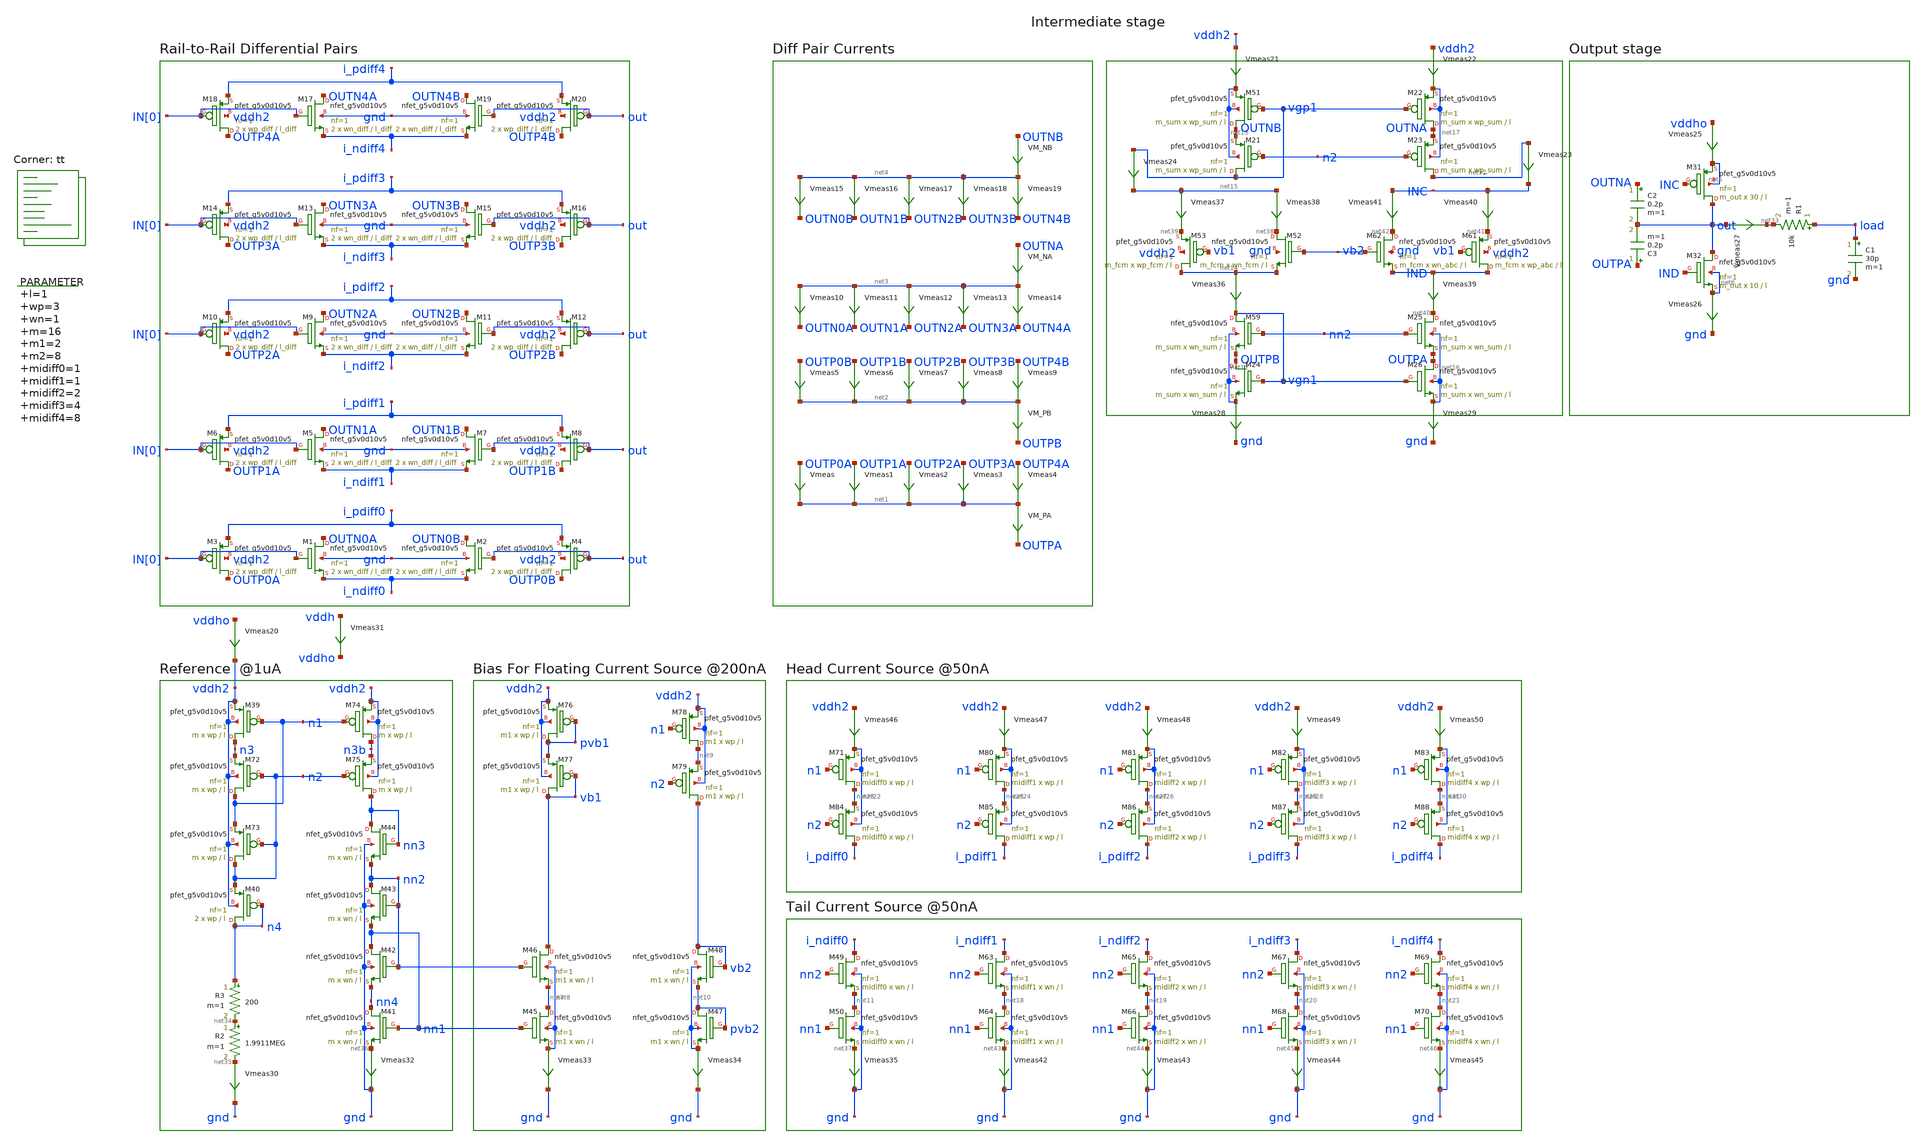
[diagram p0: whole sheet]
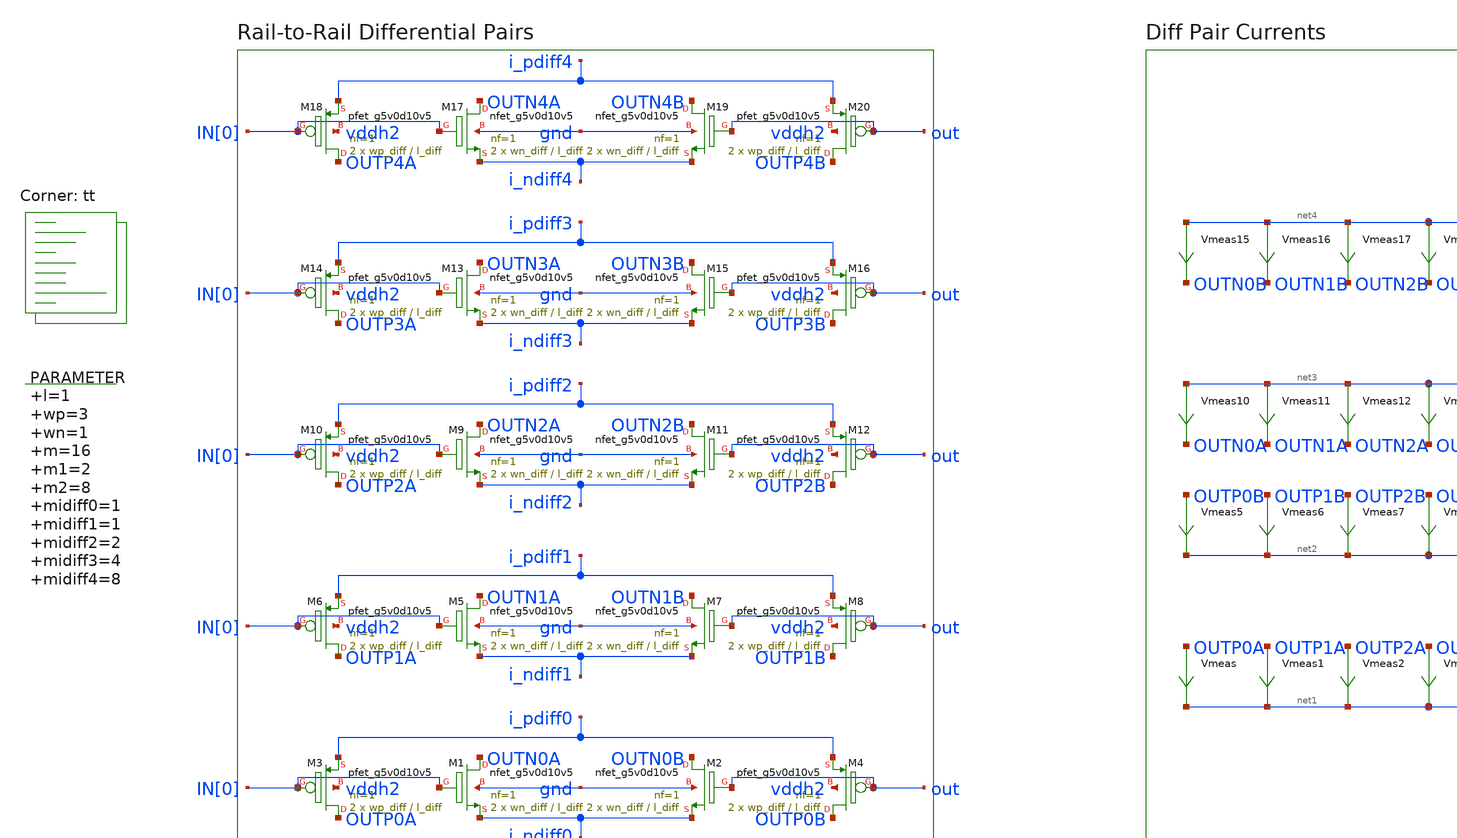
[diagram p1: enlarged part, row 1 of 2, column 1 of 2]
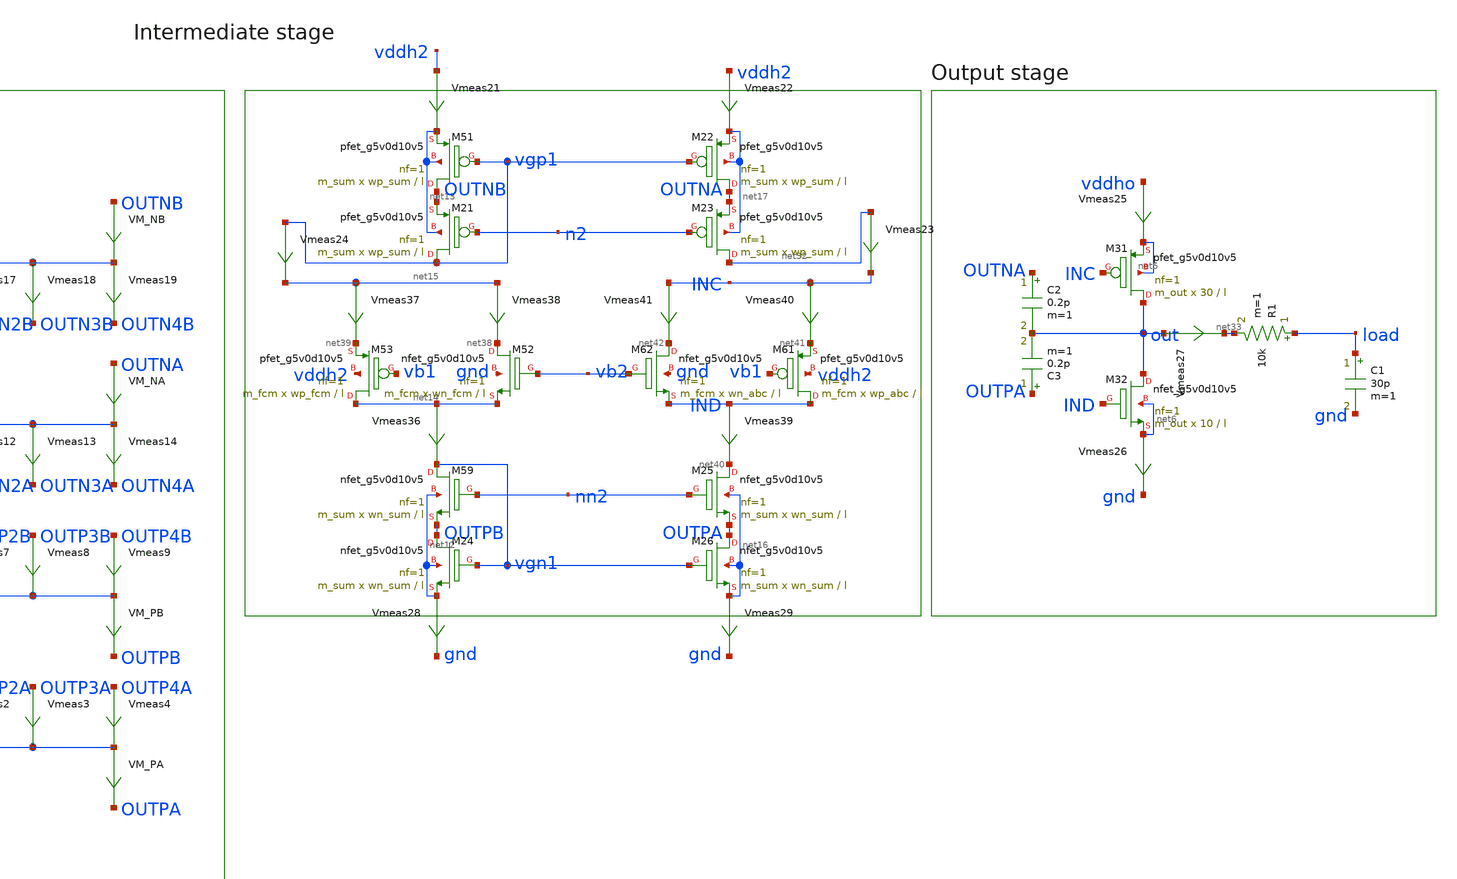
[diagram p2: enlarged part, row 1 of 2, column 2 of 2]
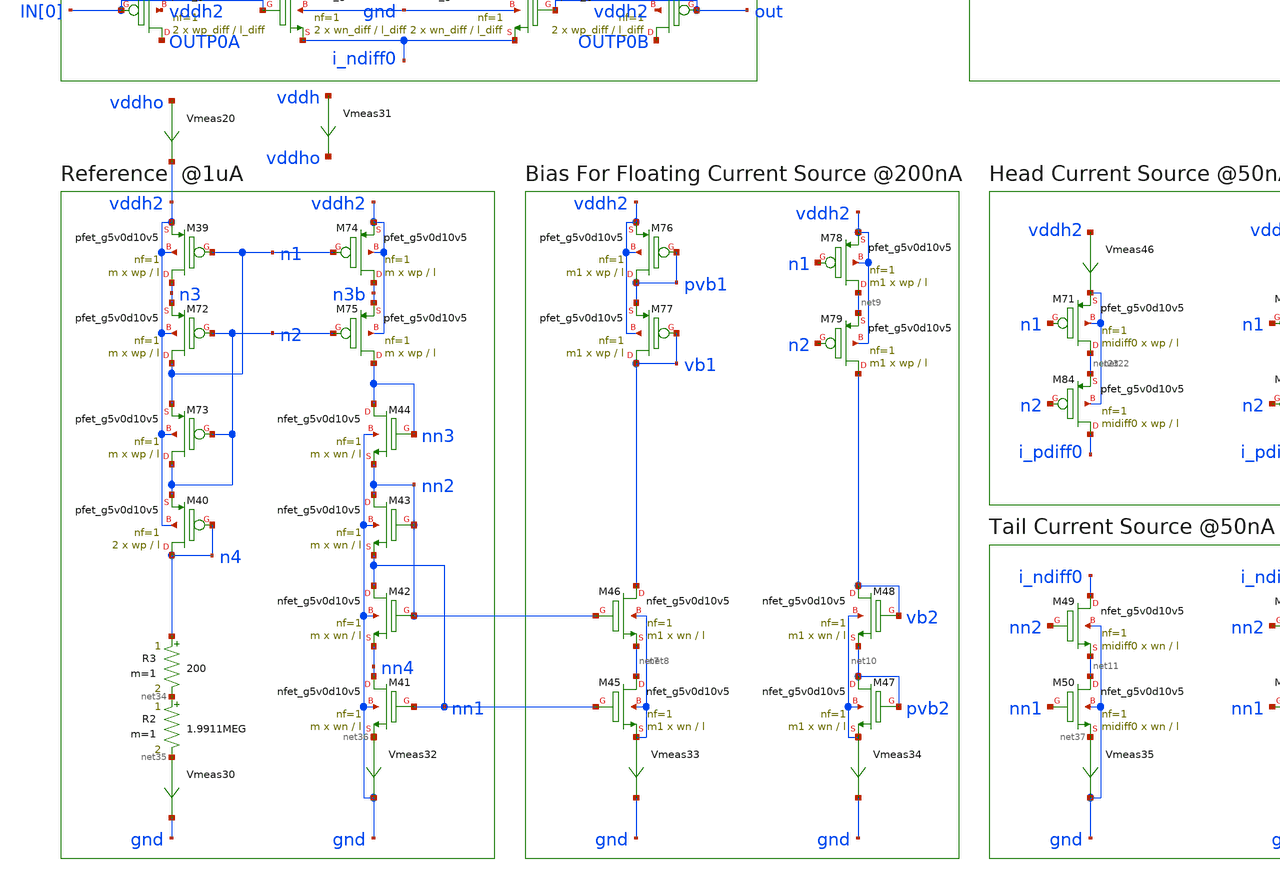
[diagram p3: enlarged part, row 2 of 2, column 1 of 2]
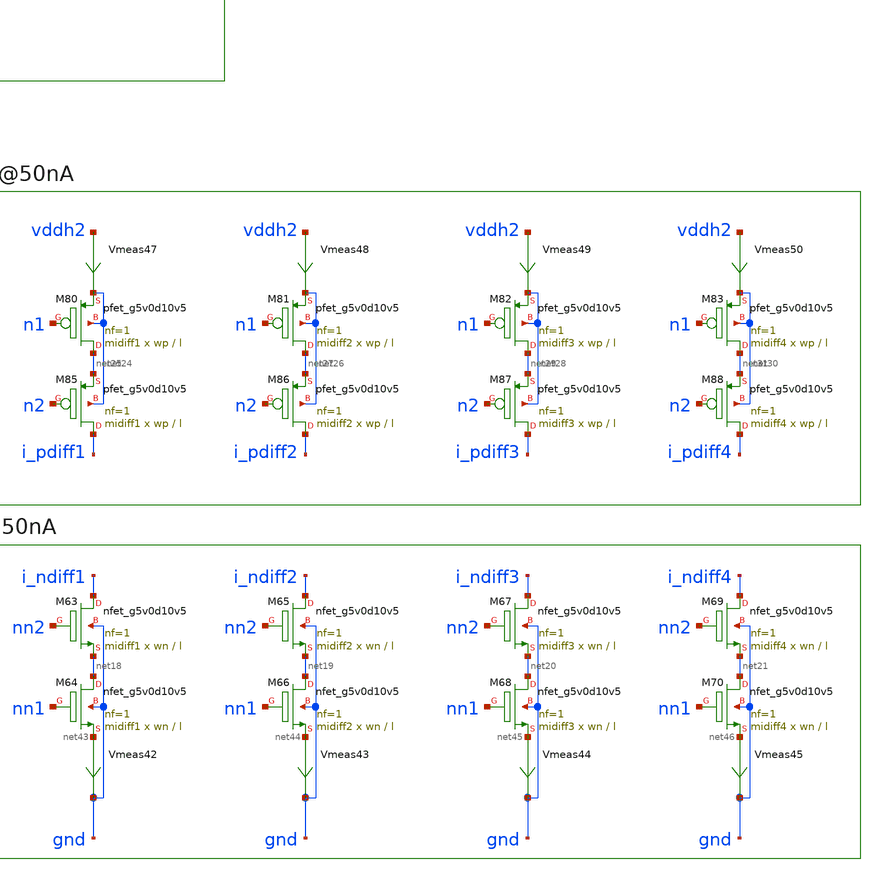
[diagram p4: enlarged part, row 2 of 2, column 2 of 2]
** sch_path: xschem/op_amp_v2-tb.sch
**.subckt op_amp_v2-tb
XM1 OUTN0A IN[0] i_ndiff0 gnd sky130_fd_pr__nfet_g5v0d10v5 L=l_diff W=wn_diff nf=1 ad='int((nf+1)/2) * W/nf * 0.29'
+ as='int((nf+2)/2) * W/nf * 0.29' pd='2*int((nf+1)/2) * (W/nf + 0.29)' ps='2*int((nf+2)/2) * (W/nf + 0.29)'
+ nrd='0.29 / W' nrs='0.29 / W' sa=0 sb=0 sd=0 mult=2 m=2
XM3 OUTP0A IN[0] i_pdiff0 vddh2 sky130_fd_pr__pfet_g5v0d10v5 L=l_diff W=wp_diff nf=1 ad='int((nf+1)/2) * W/nf * 0.29'
+ as='int((nf+2)/2) * W/nf * 0.29' pd='2*int((nf+1)/2) * (W/nf + 0.29)' ps='2*int((nf+2)/2) * (W/nf + 0.29)'
+ nrd='0.29 / W' nrs='0.29 / W' sa=0 sb=0 sd=0 mult=2 m=2
Vmeas OUTP0A net1 0
.save i(vmeas)
Vmeas1 OUTP1A net1 0
.save i(vmeas1)
Vmeas2 OUTP2A net1 0
.save i(vmeas2)
Vmeas3 OUTP3A net1 0
.save i(vmeas3)
Vmeas4 OUTP4A net1 0
.save i(vmeas4)
Vmeas5 OUTP0B net2 0
.save i(vmeas5)
Vmeas6 OUTP1B net2 0
.save i(vmeas6)
Vmeas7 OUTP2B net2 0
.save i(vmeas7)
Vmeas8 OUTP3B net2 0
.save i(vmeas8)
Vmeas9 OUTP4B net2 0
.save i(vmeas9)
Vmeas10 net3 OUTN0A 0
.save i(vmeas10)
Vmeas11 net3 OUTN1A 0
.save i(vmeas11)
Vmeas12 net3 OUTN2A 0
.save i(vmeas12)
Vmeas13 net3 OUTN3A 0
.save i(vmeas13)
Vmeas14 net3 OUTN4A 0
.save i(vmeas14)
Vmeas15 net4 OUTN0B 0
.save i(vmeas15)
Vmeas16 net4 OUTN1B 0
.save i(vmeas16)
Vmeas17 net4 OUTN2B 0
.save i(vmeas17)
Vmeas18 net4 OUTN3B 0
.save i(vmeas18)
Vmeas19 net4 OUTN4B 0
.save i(vmeas19)
XM31 out INC net5 net5 sky130_fd_pr__pfet_g5v0d10v5 L=l W=30 nf=1 ad='int((nf+1)/2) * W/nf * 0.29' as='int((nf+2)/2) * W/nf * 0.29'
+ pd='2*int((nf+1)/2) * (W/nf + 0.29)' ps='2*int((nf+2)/2) * (W/nf + 0.29)' nrd='0.29 / W' nrs='0.29 / W'
+ sa=0 sb=0 sd=0 mult=m_out m=m_out
XM32 out IND net6 net6 sky130_fd_pr__nfet_g5v0d10v5 L=l W=10 nf=1 ad='int((nf+1)/2) * W/nf * 0.29' as='int((nf+2)/2) * W/nf * 0.29'
+ pd='2*int((nf+1)/2) * (W/nf + 0.29)' ps='2*int((nf+2)/2) * (W/nf + 0.29)' nrd='0.29 / W' nrs='0.29 / W'
+ sa=0 sb=0 sd=0 mult=m_out m=m_out
R1 load net33 10k m=1
Vmeas25 vddho net5 0
.save i(vmeas25)
Vmeas26 net6 gnd 0
.save i(vmeas26)
C1 load gnd 30p m=1
VM_NB OUTNB net4 0
.save i(vm_nb)
VM_NA OUTNA net3 0
.save i(vm_na)
VM_PB net2 OUTPB 0
.save i(vm_pb)
VM_PA net1 OUTPA 0
.save i(vm_pa)
C2 OUTNA out 0.2p m=1
C3 OUTPA out 0.2p m=1
XM2 OUTN0B out i_ndiff0 gnd sky130_fd_pr__nfet_g5v0d10v5 L=l_diff W=wn_diff nf=1 ad='int((nf+1)/2) * W/nf * 0.29'
+ as='int((nf+2)/2) * W/nf * 0.29' pd='2*int((nf+1)/2) * (W/nf + 0.29)' ps='2*int((nf+2)/2) * (W/nf + 0.29)'
+ nrd='0.29 / W' nrs='0.29 / W' sa=0 sb=0 sd=0 mult=2 m=2
XM4 OUTP0B out i_pdiff0 vddh2 sky130_fd_pr__pfet_g5v0d10v5 L=l_diff W=wp_diff nf=1 ad='int((nf+1)/2) * W/nf * 0.29'
+ as='int((nf+2)/2) * W/nf * 0.29' pd='2*int((nf+1)/2) * (W/nf + 0.29)' ps='2*int((nf+2)/2) * (W/nf + 0.29)'
+ nrd='0.29 / W' nrs='0.29 / W' sa=0 sb=0 sd=0 mult=2 m=2
XM5 OUTN1A IN[0] i_ndiff1 gnd sky130_fd_pr__nfet_g5v0d10v5 L=l_diff W=wn_diff nf=1 ad='int((nf+1)/2) * W/nf * 0.29'
+ as='int((nf+2)/2) * W/nf * 0.29' pd='2*int((nf+1)/2) * (W/nf + 0.29)' ps='2*int((nf+2)/2) * (W/nf + 0.29)'
+ nrd='0.29 / W' nrs='0.29 / W' sa=0 sb=0 sd=0 mult=2 m=2
XM6 OUTP1A IN[0] i_pdiff1 vddh2 sky130_fd_pr__pfet_g5v0d10v5 L=l_diff W=wp_diff nf=1 ad='int((nf+1)/2) * W/nf * 0.29'
+ as='int((nf+2)/2) * W/nf * 0.29' pd='2*int((nf+1)/2) * (W/nf + 0.29)' ps='2*int((nf+2)/2) * (W/nf + 0.29)'
+ nrd='0.29 / W' nrs='0.29 / W' sa=0 sb=0 sd=0 mult=2 m=2
XM7 OUTN1B out i_ndiff1 gnd sky130_fd_pr__nfet_g5v0d10v5 L=l_diff W=wn_diff nf=1 ad='int((nf+1)/2) * W/nf * 0.29'
+ as='int((nf+2)/2) * W/nf * 0.29' pd='2*int((nf+1)/2) * (W/nf + 0.29)' ps='2*int((nf+2)/2) * (W/nf + 0.29)'
+ nrd='0.29 / W' nrs='0.29 / W' sa=0 sb=0 sd=0 mult=2 m=2
XM8 OUTP1B out i_pdiff1 vddh2 sky130_fd_pr__pfet_g5v0d10v5 L=l_diff W=wp_diff nf=1 ad='int((nf+1)/2) * W/nf * 0.29'
+ as='int((nf+2)/2) * W/nf * 0.29' pd='2*int((nf+1)/2) * (W/nf + 0.29)' ps='2*int((nf+2)/2) * (W/nf + 0.29)'
+ nrd='0.29 / W' nrs='0.29 / W' sa=0 sb=0 sd=0 mult=2 m=2
XM9 OUTN2A IN[0] i_ndiff2 gnd sky130_fd_pr__nfet_g5v0d10v5 L=l_diff W=wn_diff nf=1 ad='int((nf+1)/2) * W/nf * 0.29'
+ as='int((nf+2)/2) * W/nf * 0.29' pd='2*int((nf+1)/2) * (W/nf + 0.29)' ps='2*int((nf+2)/2) * (W/nf + 0.29)'
+ nrd='0.29 / W' nrs='0.29 / W' sa=0 sb=0 sd=0 mult=2 m=2
XM10 OUTP2A IN[0] i_pdiff2 vddh2 sky130_fd_pr__pfet_g5v0d10v5 L=l_diff W=wp_diff nf=1 ad='int((nf+1)/2) * W/nf * 0.29'
+ as='int((nf+2)/2) * W/nf * 0.29' pd='2*int((nf+1)/2) * (W/nf + 0.29)' ps='2*int((nf+2)/2) * (W/nf + 0.29)'
+ nrd='0.29 / W' nrs='0.29 / W' sa=0 sb=0 sd=0 mult=2 m=2
XM11 OUTN2B out i_ndiff2 gnd sky130_fd_pr__nfet_g5v0d10v5 L=l_diff W=wn_diff nf=1 ad='int((nf+1)/2) * W/nf * 0.29'
+ as='int((nf+2)/2) * W/nf * 0.29' pd='2*int((nf+1)/2) * (W/nf + 0.29)' ps='2*int((nf+2)/2) * (W/nf + 0.29)'
+ nrd='0.29 / W' nrs='0.29 / W' sa=0 sb=0 sd=0 mult=2 m=2
XM12 OUTP2B out i_pdiff2 vddh2 sky130_fd_pr__pfet_g5v0d10v5 L=l_diff W=wp_diff nf=1 ad='int((nf+1)/2) * W/nf * 0.29'
+ as='int((nf+2)/2) * W/nf * 0.29' pd='2*int((nf+1)/2) * (W/nf + 0.29)' ps='2*int((nf+2)/2) * (W/nf + 0.29)'
+ nrd='0.29 / W' nrs='0.29 / W' sa=0 sb=0 sd=0 mult=2 m=2
XM13 OUTN3A IN[0] i_ndiff3 gnd sky130_fd_pr__nfet_g5v0d10v5 L=l_diff W=wn_diff nf=1 ad='int((nf+1)/2) * W/nf * 0.29'
+ as='int((nf+2)/2) * W/nf * 0.29' pd='2*int((nf+1)/2) * (W/nf + 0.29)' ps='2*int((nf+2)/2) * (W/nf + 0.29)'
+ nrd='0.29 / W' nrs='0.29 / W' sa=0 sb=0 sd=0 mult=2 m=2
XM14 OUTP3A IN[0] i_pdiff3 vddh2 sky130_fd_pr__pfet_g5v0d10v5 L=l_diff W=wp_diff nf=1 ad='int((nf+1)/2) * W/nf * 0.29'
+ as='int((nf+2)/2) * W/nf * 0.29' pd='2*int((nf+1)/2) * (W/nf + 0.29)' ps='2*int((nf+2)/2) * (W/nf + 0.29)'
+ nrd='0.29 / W' nrs='0.29 / W' sa=0 sb=0 sd=0 mult=2 m=2
XM15 OUTN3B out i_ndiff3 gnd sky130_fd_pr__nfet_g5v0d10v5 L=l_diff W=wn_diff nf=1 ad='int((nf+1)/2) * W/nf * 0.29'
+ as='int((nf+2)/2) * W/nf * 0.29' pd='2*int((nf+1)/2) * (W/nf + 0.29)' ps='2*int((nf+2)/2) * (W/nf + 0.29)'
+ nrd='0.29 / W' nrs='0.29 / W' sa=0 sb=0 sd=0 mult=2 m=2
XM16 OUTP3B out i_pdiff3 vddh2 sky130_fd_pr__pfet_g5v0d10v5 L=l_diff W=wp_diff nf=1 ad='int((nf+1)/2) * W/nf * 0.29'
+ as='int((nf+2)/2) * W/nf * 0.29' pd='2*int((nf+1)/2) * (W/nf + 0.29)' ps='2*int((nf+2)/2) * (W/nf + 0.29)'
+ nrd='0.29 / W' nrs='0.29 / W' sa=0 sb=0 sd=0 mult=2 m=2
XM17 OUTN4A IN[0] i_ndiff4 gnd sky130_fd_pr__nfet_g5v0d10v5 L=l_diff W=wn_diff nf=1 ad='int((nf+1)/2) * W/nf * 0.29'
+ as='int((nf+2)/2) * W/nf * 0.29' pd='2*int((nf+1)/2) * (W/nf + 0.29)' ps='2*int((nf+2)/2) * (W/nf + 0.29)'
+ nrd='0.29 / W' nrs='0.29 / W' sa=0 sb=0 sd=0 mult=2 m=2
XM18 OUTP4A IN[0] i_pdiff4 vddh2 sky130_fd_pr__pfet_g5v0d10v5 L=l_diff W=wp_diff nf=1 ad='int((nf+1)/2) * W/nf * 0.29'
+ as='int((nf+2)/2) * W/nf * 0.29' pd='2*int((nf+1)/2) * (W/nf + 0.29)' ps='2*int((nf+2)/2) * (W/nf + 0.29)'
+ nrd='0.29 / W' nrs='0.29 / W' sa=0 sb=0 sd=0 mult=2 m=2
XM19 OUTN4B out i_ndiff4 gnd sky130_fd_pr__nfet_g5v0d10v5 L=l_diff W=wn_diff nf=1 ad='int((nf+1)/2) * W/nf * 0.29'
+ as='int((nf+2)/2) * W/nf * 0.29' pd='2*int((nf+1)/2) * (W/nf + 0.29)' ps='2*int((nf+2)/2) * (W/nf + 0.29)'
+ nrd='0.29 / W' nrs='0.29 / W' sa=0 sb=0 sd=0 mult=2 m=2
XM20 OUTP4B out i_pdiff4 vddh2 sky130_fd_pr__pfet_g5v0d10v5 L=l_diff W=wp_diff nf=1 ad='int((nf+1)/2) * W/nf * 0.29'
+ as='int((nf+2)/2) * W/nf * 0.29' pd='2*int((nf+1)/2) * (W/nf + 0.29)' ps='2*int((nf+2)/2) * (W/nf + 0.29)'
+ nrd='0.29 / W' nrs='0.29 / W' sa=0 sb=0 sd=0 mult=2 m=2
XM39 n3 n1 vddh2 vddh2 sky130_fd_pr__pfet_g5v0d10v5 L=l W=wp nf=1 ad='int((nf+1)/2) * W/nf * 0.29' as='int((nf+2)/2) * W/nf * 0.29'
+ pd='2*int((nf+1)/2) * (W/nf + 0.29)' ps='2*int((nf+2)/2) * (W/nf + 0.29)' nrd='0.29 / W' nrs='0.29 / W'
+ sa=0 sb=0 sd=0 mult=m m=m
R2 net34 net35 1.9911MEG m=1
Vmeas30 net35 gnd 0
.save i(vmeas30)
R3 n4 net34 200 m=1
XM40 n4 n4 n2 vddh2 sky130_fd_pr__pfet_g5v0d10v5 L=l W=wp nf=1 ad='int((nf+1)/2) * W/nf * 0.29' as='int((nf+2)/2) * W/nf * 0.29'
+ pd='2*int((nf+1)/2) * (W/nf + 0.29)' ps='2*int((nf+2)/2) * (W/nf + 0.29)' nrd='0.29 / W' nrs='0.29 / W'
+ sa=0 sb=0 sd=0 mult=2 m=2
Vmeas31 vddh vddho 0
.save i(vmeas31)
XM41 nn4 nn1 net36 gnd sky130_fd_pr__nfet_g5v0d10v5 L=l W=wn nf=1 ad='int((nf+1)/2) * W/nf * 0.29' as='int((nf+2)/2) * W/nf * 0.29'
+ pd='2*int((nf+1)/2) * (W/nf + 0.29)' ps='2*int((nf+2)/2) * (W/nf + 0.29)' nrd='0.29 / W' nrs='0.29 / W'
+ sa=0 sb=0 sd=0 mult=m m=m
XM42 nn1 nn2 nn4 gnd sky130_fd_pr__nfet_g5v0d10v5 L=l W=wn nf=1 ad='int((nf+1)/2) * W/nf * 0.29' as='int((nf+2)/2) * W/nf * 0.29'
+ pd='2*int((nf+1)/2) * (W/nf + 0.29)' ps='2*int((nf+2)/2) * (W/nf + 0.29)' nrd='0.29 / W' nrs='0.29 / W'
+ sa=0 sb=0 sd=0 mult=m m=m
XM43 nn2 nn2 nn1 gnd sky130_fd_pr__nfet_g5v0d10v5 L=l W=wn nf=1 ad='int((nf+1)/2) * W/nf * 0.29' as='int((nf+2)/2) * W/nf * 0.29'
+ pd='2*int((nf+1)/2) * (W/nf + 0.29)' ps='2*int((nf+2)/2) * (W/nf + 0.29)' nrd='0.29 / W' nrs='0.29 / W'
+ sa=0 sb=0 sd=0 mult=m m=m
XM44 nn3 nn3 nn2 gnd sky130_fd_pr__nfet_g5v0d10v5 L=l W=wn nf=1 ad='int((nf+1)/2) * W/nf * 0.29' as='int((nf+2)/2) * W/nf * 0.29'
+ pd='2*int((nf+1)/2) * (W/nf + 0.29)' ps='2*int((nf+2)/2) * (W/nf + 0.29)' nrd='0.29 / W' nrs='0.29 / W'
+ sa=0 sb=0 sd=0 mult=m m=m
Vmeas32 net36 gnd 0
.save i(vmeas32)
XM45 net7 nn1 net8 net8 sky130_fd_pr__nfet_g5v0d10v5 L=l W=wn nf=1 ad='int((nf+1)/2) * W/nf * 0.29' as='int((nf+2)/2) * W/nf * 0.29'
+ pd='2*int((nf+1)/2) * (W/nf + 0.29)' ps='2*int((nf+2)/2) * (W/nf + 0.29)' nrd='0.29 / W' nrs='0.29 / W'
+ sa=0 sb=0 sd=0 mult=m1 m=m1
XM46 vb1 nn2 net7 net8 sky130_fd_pr__nfet_g5v0d10v5 L=l W=wn nf=1 ad='int((nf+1)/2) * W/nf * 0.29' as='int((nf+2)/2) * W/nf * 0.29'
+ pd='2*int((nf+1)/2) * (W/nf + 0.29)' ps='2*int((nf+2)/2) * (W/nf + 0.29)' nrd='0.29 / W' nrs='0.29 / W'
+ sa=0 sb=0 sd=0 mult=m1 m=m1
Vmeas33 net8 gnd 0
.save i(vmeas33)
XM47 pvb2 pvb2 net10 net10 sky130_fd_pr__nfet_g5v0d10v5 L=l W=wn nf=1 ad='int((nf+1)/2) * W/nf * 0.29'
+ as='int((nf+2)/2) * W/nf * 0.29' pd='2*int((nf+1)/2) * (W/nf + 0.29)' ps='2*int((nf+2)/2) * (W/nf + 0.29)'
+ nrd='0.29 / W' nrs='0.29 / W' sa=0 sb=0 sd=0 mult=m1 m=m1
XM48 vb2 vb2 pvb2 net10 sky130_fd_pr__nfet_g5v0d10v5 L=l W=wn nf=1 ad='int((nf+1)/2) * W/nf * 0.29' as='int((nf+2)/2) * W/nf * 0.29'
+ pd='2*int((nf+1)/2) * (W/nf + 0.29)' ps='2*int((nf+2)/2) * (W/nf + 0.29)' nrd='0.29 / W' nrs='0.29 / W'
+ sa=0 sb=0 sd=0 mult=m1 m=m1
Vmeas34 net10 gnd 0
.save i(vmeas34)
XM49 i_ndiff0 nn2 net11 gnd sky130_fd_pr__nfet_g5v0d10v5 L=l W=wn nf=1 ad='int((nf+1)/2) * W/nf * 0.29'
+ as='int((nf+2)/2) * W/nf * 0.29' pd='2*int((nf+1)/2) * (W/nf + 0.29)' ps='2*int((nf+2)/2) * (W/nf + 0.29)'
+ nrd='0.29 / W' nrs='0.29 / W' sa=0 sb=0 sd=0 mult=midiff0 m=midiff0
XM50 net11 nn1 net37 gnd sky130_fd_pr__nfet_g5v0d10v5 L=l W=wn nf=1 ad='int((nf+1)/2) * W/nf * 0.29'
+ as='int((nf+2)/2) * W/nf * 0.29' pd='2*int((nf+1)/2) * (W/nf + 0.29)' ps='2*int((nf+2)/2) * (W/nf + 0.29)'
+ nrd='0.29 / W' nrs='0.29 / W' sa=0 sb=0 sd=0 mult=midiff0 m=midiff0
Vmeas35 net37 gnd 0
.save i(vmeas35)
Vmeas36 net14 vgn1 0
.save i(vmeas36)
XM51 OUTNB vgp1 net13 net13 sky130_fd_pr__pfet_g5v0d10v5 L=l W=wp_sum nf=1 ad='int((nf+1)/2) * W/nf * 0.29'
+ as='int((nf+2)/2) * W/nf * 0.29' pd='2*int((nf+1)/2) * (W/nf + 0.29)' ps='2*int((nf+2)/2) * (W/nf + 0.29)'
+ nrd='0.29 / W' nrs='0.29 / W' sa=0 sb=0 sd=0 mult=m_sum m=m_sum
XM52 net38 vb2 net14 gnd sky130_fd_pr__nfet_g5v0d10v5 L=l W=wn_fcm nf=1 ad='int((nf+1)/2) * W/nf * 0.29'
+ as='int((nf+2)/2) * W/nf * 0.29' pd='2*int((nf+1)/2) * (W/nf + 0.29)' ps='2*int((nf+2)/2) * (W/nf + 0.29)'
+ nrd='0.29 / W' nrs='0.29 / W' sa=0 sb=0 sd=0 mult=m_fcm m=m_fcm
Vmeas37 net15 net39 0
.save i(vmeas37)
Vmeas38 net15 net38 0
.save i(vmeas38)
XM53 net14 vb1 net39 vddh2 sky130_fd_pr__pfet_g5v0d10v5 L=l W=wp_fcm nf=1 ad='int((nf+1)/2) * W/nf * 0.29'
+ as='int((nf+2)/2) * W/nf * 0.29' pd='2*int((nf+1)/2) * (W/nf + 0.29)' ps='2*int((nf+2)/2) * (W/nf + 0.29)'
+ nrd='0.29 / W' nrs='0.29 / W' sa=0 sb=0 sd=0 mult=m_fcm m=m_fcm
Vmeas39 IND net40 0
.save i(vmeas39)
Vmeas40 INC net41 0
.save i(vmeas40)
Vmeas41 INC net42 0
.save i(vmeas41)
XM59 vgn1 nn2 OUTPB net12 sky130_fd_pr__nfet_g5v0d10v5 L=l W=wn_sum nf=1 ad='int((nf+1)/2) * W/nf * 0.29'
+ as='int((nf+2)/2) * W/nf * 0.29' pd='2*int((nf+1)/2) * (W/nf + 0.29)' ps='2*int((nf+2)/2) * (W/nf + 0.29)'
+ nrd='0.29 / W' nrs='0.29 / W' sa=0 sb=0 sd=0 mult=m_sum m=m_sum
XM61 IND vb1 net41 vddh2 sky130_fd_pr__pfet_g5v0d10v5 L=l W=wp_abc nf=1 ad='int((nf+1)/2) * W/nf * 0.29'
+ as='int((nf+2)/2) * W/nf * 0.29' pd='2*int((nf+1)/2) * (W/nf + 0.29)' ps='2*int((nf+2)/2) * (W/nf + 0.29)'
+ nrd='0.29 / W' nrs='0.29 / W' sa=0 sb=0 sd=0 mult=m_fcm m=m_fcm
XM62 net42 vb2 IND gnd sky130_fd_pr__nfet_g5v0d10v5 L=l W=wn_abc nf=1 ad='int((nf+1)/2) * W/nf * 0.29'
+ as='int((nf+2)/2) * W/nf * 0.29' pd='2*int((nf+1)/2) * (W/nf + 0.29)' ps='2*int((nf+2)/2) * (W/nf + 0.29)'
+ nrd='0.29 / W' nrs='0.29 / W' sa=0 sb=0 sd=0 mult=m_fcm m=m_fcm
XM63 i_ndiff1 nn2 net18 gnd sky130_fd_pr__nfet_g5v0d10v5 L=l W=wn nf=1 ad='int((nf+1)/2) * W/nf * 0.29'
+ as='int((nf+2)/2) * W/nf * 0.29' pd='2*int((nf+1)/2) * (W/nf + 0.29)' ps='2*int((nf+2)/2) * (W/nf + 0.29)'
+ nrd='0.29 / W' nrs='0.29 / W' sa=0 sb=0 sd=0 mult=midiff1 m=midiff1
XM64 net18 nn1 net43 gnd sky130_fd_pr__nfet_g5v0d10v5 L=l W=wn nf=1 ad='int((nf+1)/2) * W/nf * 0.29'
+ as='int((nf+2)/2) * W/nf * 0.29' pd='2*int((nf+1)/2) * (W/nf + 0.29)' ps='2*int((nf+2)/2) * (W/nf + 0.29)'
+ nrd='0.29 / W' nrs='0.29 / W' sa=0 sb=0 sd=0 mult=midiff1 m=midiff1
Vmeas42 net43 gnd 0
.save i(vmeas42)
XM65 i_ndiff2 nn2 net19 gnd sky130_fd_pr__nfet_g5v0d10v5 L=l W=wn nf=1 ad='int((nf+1)/2) * W/nf * 0.29'
+ as='int((nf+2)/2) * W/nf * 0.29' pd='2*int((nf+1)/2) * (W/nf + 0.29)' ps='2*int((nf+2)/2) * (W/nf + 0.29)'
+ nrd='0.29 / W' nrs='0.29 / W' sa=0 sb=0 sd=0 mult=midiff2 m=midiff2
XM66 net19 nn1 net44 gnd sky130_fd_pr__nfet_g5v0d10v5 L=l W=wn nf=1 ad='int((nf+1)/2) * W/nf * 0.29'
+ as='int((nf+2)/2) * W/nf * 0.29' pd='2*int((nf+1)/2) * (W/nf + 0.29)' ps='2*int((nf+2)/2) * (W/nf + 0.29)'
+ nrd='0.29 / W' nrs='0.29 / W' sa=0 sb=0 sd=0 mult=midiff2 m=midiff2
Vmeas43 net44 gnd 0
.save i(vmeas43)
XM67 i_ndiff3 nn2 net20 gnd sky130_fd_pr__nfet_g5v0d10v5 L=l W=wn nf=1 ad='int((nf+1)/2) * W/nf * 0.29'
+ as='int((nf+2)/2) * W/nf * 0.29' pd='2*int((nf+1)/2) * (W/nf + 0.29)' ps='2*int((nf+2)/2) * (W/nf + 0.29)'
+ nrd='0.29 / W' nrs='0.29 / W' sa=0 sb=0 sd=0 mult=midiff3 m=midiff3
XM68 net20 nn1 net45 gnd sky130_fd_pr__nfet_g5v0d10v5 L=l W=wn nf=1 ad='int((nf+1)/2) * W/nf * 0.29'
+ as='int((nf+2)/2) * W/nf * 0.29' pd='2*int((nf+1)/2) * (W/nf + 0.29)' ps='2*int((nf+2)/2) * (W/nf + 0.29)'
+ nrd='0.29 / W' nrs='0.29 / W' sa=0 sb=0 sd=0 mult=midiff3 m=midiff3
Vmeas44 net45 gnd 0
.save i(vmeas44)
XM69 i_ndiff4 nn2 net21 gnd sky130_fd_pr__nfet_g5v0d10v5 L=l W=wn nf=1 ad='int((nf+1)/2) * W/nf * 0.29'
+ as='int((nf+2)/2) * W/nf * 0.29' pd='2*int((nf+1)/2) * (W/nf + 0.29)' ps='2*int((nf+2)/2) * (W/nf + 0.29)'
+ nrd='0.29 / W' nrs='0.29 / W' sa=0 sb=0 sd=0 mult=midiff4 m=midiff4
XM70 net21 nn1 net46 gnd sky130_fd_pr__nfet_g5v0d10v5 L=l W=wn nf=1 ad='int((nf+1)/2) * W/nf * 0.29'
+ as='int((nf+2)/2) * W/nf * 0.29' pd='2*int((nf+1)/2) * (W/nf + 0.29)' ps='2*int((nf+2)/2) * (W/nf + 0.29)'
+ nrd='0.29 / W' nrs='0.29 / W' sa=0 sb=0 sd=0 mult=midiff4 m=midiff4
Vmeas45 net46 gnd 0
.save i(vmeas45)
XM71 net23 n1 net22 net22 sky130_fd_pr__pfet_g5v0d10v5 L=l W=wp nf=1 ad='int((nf+1)/2) * W/nf * 0.29'
+ as='int((nf+2)/2) * W/nf * 0.29' pd='2*int((nf+1)/2) * (W/nf + 0.29)' ps='2*int((nf+2)/2) * (W/nf + 0.29)'
+ nrd='0.29 / W' nrs='0.29 / W' sa=0 sb=0 sd=0 mult=midiff0 m=midiff0
Vmeas46 vddh2 net22 0
.save i(vmeas46)
XM72 n1 n2 n3 vddh2 sky130_fd_pr__pfet_g5v0d10v5 L=l W=wp nf=1 ad='int((nf+1)/2) * W/nf * 0.29' as='int((nf+2)/2) * W/nf * 0.29'
+ pd='2*int((nf+1)/2) * (W/nf + 0.29)' ps='2*int((nf+2)/2) * (W/nf + 0.29)' nrd='0.29 / W' nrs='0.29 / W'
+ sa=0 sb=0 sd=0 mult=m m=m
XM73 n2 n2 n1 vddh2 sky130_fd_pr__pfet_g5v0d10v5 L=l W=wp nf=1 ad='int((nf+1)/2) * W/nf * 0.29' as='int((nf+2)/2) * W/nf * 0.29'
+ pd='2*int((nf+1)/2) * (W/nf + 0.29)' ps='2*int((nf+2)/2) * (W/nf + 0.29)' nrd='0.29 / W' nrs='0.29 / W'
+ sa=0 sb=0 sd=0 mult=m m=m
XM74 n3b n1 vddh2 vddh2 sky130_fd_pr__pfet_g5v0d10v5 L=l W=wp nf=1 ad='int((nf+1)/2) * W/nf * 0.29' as='int((nf+2)/2) * W/nf * 0.29'
+ pd='2*int((nf+1)/2) * (W/nf + 0.29)' ps='2*int((nf+2)/2) * (W/nf + 0.29)' nrd='0.29 / W' nrs='0.29 / W'
+ sa=0 sb=0 sd=0 mult=m m=m
XM75 nn3 n2 n3b vddh2 sky130_fd_pr__pfet_g5v0d10v5 L=l W=wp nf=1 ad='int((nf+1)/2) * W/nf * 0.29' as='int((nf+2)/2) * W/nf * 0.29'
+ pd='2*int((nf+1)/2) * (W/nf + 0.29)' ps='2*int((nf+2)/2) * (W/nf + 0.29)' nrd='0.29 / W' nrs='0.29 / W'
+ sa=0 sb=0 sd=0 mult=m m=m
XM76 pvb1 pvb1 vddh2 vddh2 sky130_fd_pr__pfet_g5v0d10v5 L=l W=wp nf=1 ad='int((nf+1)/2) * W/nf * 0.29'
+ as='int((nf+2)/2) * W/nf * 0.29' pd='2*int((nf+1)/2) * (W/nf + 0.29)' ps='2*int((nf+2)/2) * (W/nf + 0.29)'
+ nrd='0.29 / W' nrs='0.29 / W' sa=0 sb=0 sd=0 mult=m1 m=m1
XM77 vb1 vb1 pvb1 vddh2 sky130_fd_pr__pfet_g5v0d10v5 L=l W=wp nf=1 ad='int((nf+1)/2) * W/nf * 0.29' as='int((nf+2)/2) * W/nf * 0.29'
+ pd='2*int((nf+1)/2) * (W/nf + 0.29)' ps='2*int((nf+2)/2) * (W/nf + 0.29)' nrd='0.29 / W' nrs='0.29 / W'
+ sa=0 sb=0 sd=0 mult=m1 m=m1
XM78 net9 n1 vddh2 vddh2 sky130_fd_pr__pfet_g5v0d10v5 L=l W=wp nf=1 ad='int((nf+1)/2) * W/nf * 0.29'
+ as='int((nf+2)/2) * W/nf * 0.29' pd='2*int((nf+1)/2) * (W/nf + 0.29)' ps='2*int((nf+2)/2) * (W/nf + 0.29)'
+ nrd='0.29 / W' nrs='0.29 / W' sa=0 sb=0 sd=0 mult=m1 m=m1
XM79 vb2 n2 net9 vddh2 sky130_fd_pr__pfet_g5v0d10v5 L=l W=wp nf=1 ad='int((nf+1)/2) * W/nf * 0.29' as='int((nf+2)/2) * W/nf * 0.29'
+ pd='2*int((nf+1)/2) * (W/nf + 0.29)' ps='2*int((nf+2)/2) * (W/nf + 0.29)' nrd='0.29 / W' nrs='0.29 / W'
+ sa=0 sb=0 sd=0 mult=m1 m=m1
XM80 net25 n1 net24 net24 sky130_fd_pr__pfet_g5v0d10v5 L=l W=wp nf=1 ad='int((nf+1)/2) * W/nf * 0.29'
+ as='int((nf+2)/2) * W/nf * 0.29' pd='2*int((nf+1)/2) * (W/nf + 0.29)' ps='2*int((nf+2)/2) * (W/nf + 0.29)'
+ nrd='0.29 / W' nrs='0.29 / W' sa=0 sb=0 sd=0 mult=midiff1 m=midiff1
Vmeas47 vddh2 net24 0
.save i(vmeas47)
XM81 net27 n1 net26 net26 sky130_fd_pr__pfet_g5v0d10v5 L=l W=wp nf=1 ad='int((nf+1)/2) * W/nf * 0.29'
+ as='int((nf+2)/2) * W/nf * 0.29' pd='2*int((nf+1)/2) * (W/nf + 0.29)' ps='2*int((nf+2)/2) * (W/nf + 0.29)'
+ nrd='0.29 / W' nrs='0.29 / W' sa=0 sb=0 sd=0 mult=midiff2 m=midiff2
Vmeas48 vddh2 net26 0
.save i(vmeas48)
XM82 net29 n1 net28 net28 sky130_fd_pr__pfet_g5v0d10v5 L=l W=wp nf=1 ad='int((nf+1)/2) * W/nf * 0.29'
+ as='int((nf+2)/2) * W/nf * 0.29' pd='2*int((nf+1)/2) * (W/nf + 0.29)' ps='2*int((nf+2)/2) * (W/nf + 0.29)'
+ nrd='0.29 / W' nrs='0.29 / W' sa=0 sb=0 sd=0 mult=midiff3 m=midiff3
Vmeas49 vddh2 net28 0
.save i(vmeas49)
XM83 net31 n1 net30 net30 sky130_fd_pr__pfet_g5v0d10v5 L=l W=wp nf=1 ad='int((nf+1)/2) * W/nf * 0.29'
+ as='int((nf+2)/2) * W/nf * 0.29' pd='2*int((nf+1)/2) * (W/nf + 0.29)' ps='2*int((nf+2)/2) * (W/nf + 0.29)'
+ nrd='0.29 / W' nrs='0.29 / W' sa=0 sb=0 sd=0 mult=midiff4 m=midiff4
Vmeas50 vddh2 net30 0
.save i(vmeas50)
XM84 i_pdiff0 n2 net23 net22 sky130_fd_pr__pfet_g5v0d10v5 L=l W=wp nf=1 ad='int((nf+1)/2) * W/nf * 0.29'
+ as='int((nf+2)/2) * W/nf * 0.29' pd='2*int((nf+1)/2) * (W/nf + 0.29)' ps='2*int((nf+2)/2) * (W/nf + 0.29)'
+ nrd='0.29 / W' nrs='0.29 / W' sa=0 sb=0 sd=0 mult=midiff0 m=midiff0
XM85 i_pdiff1 n2 net25 net24 sky130_fd_pr__pfet_g5v0d10v5 L=l W=wp nf=1 ad='int((nf+1)/2) * W/nf * 0.29'
+ as='int((nf+2)/2) * W/nf * 0.29' pd='2*int((nf+1)/2) * (W/nf + 0.29)' ps='2*int((nf+2)/2) * (W/nf + 0.29)'
+ nrd='0.29 / W' nrs='0.29 / W' sa=0 sb=0 sd=0 mult=midiff1 m=midiff1
XM86 i_pdiff2 n2 net27 net26 sky130_fd_pr__pfet_g5v0d10v5 L=l W=wp nf=1 ad='int((nf+1)/2) * W/nf * 0.29'
+ as='int((nf+2)/2) * W/nf * 0.29' pd='2*int((nf+1)/2) * (W/nf + 0.29)' ps='2*int((nf+2)/2) * (W/nf + 0.29)'
+ nrd='0.29 / W' nrs='0.29 / W' sa=0 sb=0 sd=0 mult=midiff2 m=midiff2
XM87 i_pdiff3 n2 net29 net28 sky130_fd_pr__pfet_g5v0d10v5 L=l W=wp nf=1 ad='int((nf+1)/2) * W/nf * 0.29'
+ as='int((nf+2)/2) * W/nf * 0.29' pd='2*int((nf+1)/2) * (W/nf + 0.29)' ps='2*int((nf+2)/2) * (W/nf + 0.29)'
+ nrd='0.29 / W' nrs='0.29 / W' sa=0 sb=0 sd=0 mult=midiff3 m=midiff3
XM88 i_pdiff4 n2 net31 net30 sky130_fd_pr__pfet_g5v0d10v5 L=l W=wp nf=1 ad='int((nf+1)/2) * W/nf * 0.29'
+ as='int((nf+2)/2) * W/nf * 0.29' pd='2*int((nf+1)/2) * (W/nf + 0.29)' ps='2*int((nf+2)/2) * (W/nf + 0.29)'
+ nrd='0.29 / W' nrs='0.29 / W' sa=0 sb=0 sd=0 mult=midiff4 m=midiff4
.param l=1 wp=3 wn=1 m=16 m1=2 m2=8 midiff0=1 midiff1=1 midiff2=2 midiff3=4 midiff4=8 m_sum=2
+ m_fcm=2 wp_diff=3 wn_diff=1 l_diff=1 mdiff=2 m_out=2 wp_sum=15 wn_sum=5 wp_fcm=6 wn_fcm=2 wp_abc=6 wn_abc=2
XM21 vgp1 n2 OUTNB net13 sky130_fd_pr__pfet_g5v0d10v5 L=l W=wp_sum nf=1 ad='int((nf+1)/2) * W/nf * 0.29'
+ as='int((nf+2)/2) * W/nf * 0.29' pd='2*int((nf+1)/2) * (W/nf + 0.29)' ps='2*int((nf+2)/2) * (W/nf + 0.29)'
+ nrd='0.29 / W' nrs='0.29 / W' sa=0 sb=0 sd=0 mult=m_sum m=m_sum
XM22 OUTNA vgp1 net17 net17 sky130_fd_pr__pfet_g5v0d10v5 L=l W=wp_sum nf=1 ad='int((nf+1)/2) * W/nf * 0.29'
+ as='int((nf+2)/2) * W/nf * 0.29' pd='2*int((nf+1)/2) * (W/nf + 0.29)' ps='2*int((nf+2)/2) * (W/nf + 0.29)'
+ nrd='0.29 / W' nrs='0.29 / W' sa=0 sb=0 sd=0 mult=m_sum m=m_sum
XM23 net32 n2 OUTNA net17 sky130_fd_pr__pfet_g5v0d10v5 L=l W=wp_sum nf=1 ad='int((nf+1)/2) * W/nf * 0.29'
+ as='int((nf+2)/2) * W/nf * 0.29' pd='2*int((nf+1)/2) * (W/nf + 0.29)' ps='2*int((nf+2)/2) * (W/nf + 0.29)'
+ nrd='0.29 / W' nrs='0.29 / W' sa=0 sb=0 sd=0 mult=m_sum m=m_sum
XM24 OUTPB vgn1 net12 net12 sky130_fd_pr__nfet_g5v0d10v5 L=l W=wn_sum nf=1 ad='int((nf+1)/2) * W/nf * 0.29'
+ as='int((nf+2)/2) * W/nf * 0.29' pd='2*int((nf+1)/2) * (W/nf + 0.29)' ps='2*int((nf+2)/2) * (W/nf + 0.29)'
+ nrd='0.29 / W' nrs='0.29 / W' sa=0 sb=0 sd=0 mult=m_sum m=m_sum
XM25 net40 nn2 OUTPA net16 sky130_fd_pr__nfet_g5v0d10v5 L=l W=wn_sum nf=1 ad='int((nf+1)/2) * W/nf * 0.29'
+ as='int((nf+2)/2) * W/nf * 0.29' pd='2*int((nf+1)/2) * (W/nf + 0.29)' ps='2*int((nf+2)/2) * (W/nf + 0.29)'
+ nrd='0.29 / W' nrs='0.29 / W' sa=0 sb=0 sd=0 mult=m_sum m=m_sum
XM26 OUTPA vgn1 net16 net16 sky130_fd_pr__nfet_g5v0d10v5 L=l W=wn_sum nf=1 ad='int((nf+1)/2) * W/nf * 0.29'
+ as='int((nf+2)/2) * W/nf * 0.29' pd='2*int((nf+1)/2) * (W/nf + 0.29)' ps='2*int((nf+2)/2) * (W/nf + 0.29)'
+ nrd='0.29 / W' nrs='0.29 / W' sa=0 sb=0 sd=0 mult=m_sum m=m_sum
Vmeas20 vddho vddh2 0
.save i(vmeas20)
Vmeas21 vddh2 net13 0
.save i(vmeas21)
Vmeas22 vddh2 net17 0
.save i(vmeas22)
Vmeas23 net32 INC 0
.save i(vmeas23)
Vmeas24 vgp1 net15 0
.save i(vmeas24)
Vmeas27 out net33 0
.save i(vmeas27)
Vmeas28 net12 gnd 0
.save i(vmeas28)
Vmeas29 net16 gnd 0
.save i(vmeas29)
**** begin user architecture code
.lib $::SKYWATER_MODELS/sky130.lib.spice tt



  .option wnflag=1
  .option safecurrents
  ********************Static Current Sources***************************
  .param base_current=50n
  .param i0=base_current i1={1*i0} i2={2*i0} i3={4*i0} i4={8*i0}
  *Ip0 vddh ip0 i0
  *In0 in0  gnd i0

  *Ip1 vddh ip1 i1
  *In1 in1  gnd i1

  *Ip2 vddh ip2 i2
  *In2 in2  gnd i2

  *Ip3 vddh ip3 i3
  *In3 in3  gnd i3

  *Ip4 vddh ip4 i4
  *In4 in4  gnd i4

  *Ivp vp gnd 0.2u
  *Ivn vddh vn 0.2u
  ********************Static Voltage Sources***************************
  Vddh vddh gnd dc 5.5

  *vb1 vb1 gnd dc 3.2
  *vb2 vb2 gnd dc 2.1

  *vina ina gnd sin({5.5/2} {5.5/2} 100k)
  *vinb inb gnd sin({5.5/2} {-5.5/2} 100k)

  .param vin_val=4.661
  *vin0 in[0] gnd dc vin_val
  *vin1 in[1] gnd dc vin_val
  *vin2 in[2] gnd dc vin_val
  *vin3 in[3] gnd dc vin_val
  *vin4 in[4] gnd dc vin_val
  ********************Dynamic Voltage Sources***************************
  *******Calculation**********
  .param base_f=100e3 base_t={1/base_f} base_th={base_t/2} base_d={base_th}
  .param b0_th={base_th} b0_t={b0_th*2}
  .param b1_th={b0_th*2} b1_t={b1_th*2}
  .param b2_th={b1_th*2} b2_t={b2_th*2}
  .param b3_th={b2_th*2} b3_t={b3_th*2}
  *******Signals**********
  .param vh=1.162 vl=1.044
  vin0 in[0] gnd dc pulse(5.5 0 {base_d} 1n 1n {b0_th} {b0_t})
  *vin0 in[0] gnd dc vl
  *Vin1 in[1] gnd pulse({vh} {vl} {base_d} 1n 1n {b0_th} {b0_t})
  *Vin2 in[2] gnd pulse({vh} {vl} {base_d} 1n 1n {b1_th} {b1_t})
  *Vin3 in[3] gnd pulse({vh} {vl} {base_d} 1n 1n {b2_th} {b2_t})
  *Vin4 in[4] gnd pulse({vh} {vl} {base_d} 1n 1n {b3_th} {b3_t})
  ********************Simulation Commands*****************************
  .control
     reset
     save all
     tran 1n 30u
     *dc vin0 -1 6.5 0.01
     *dc R2 1.9meg 2.1meg 10

     *ac dec 100 1 1e9

     let vout_mag =abs(v(out))
     let vout_phase_margin = phase(v(out))*180/pi + 180
     meas ac Aol find vout_mag at = 10
     meas ac UGF when vout_mag=1 fall=1
     meas ac PM find vout_phase_margin when vout_mag=1
     let difference = v(inc) - v(ind)
     save difference
     write op_amp_v2-tb.raw
     wrdata /home/yohanes/10-bit-DAC/simulations/op_amp2-tb.txt out load
     set appendwrite
*    quit 0
  .endc



**** end user architecture code
**.ends
.end
